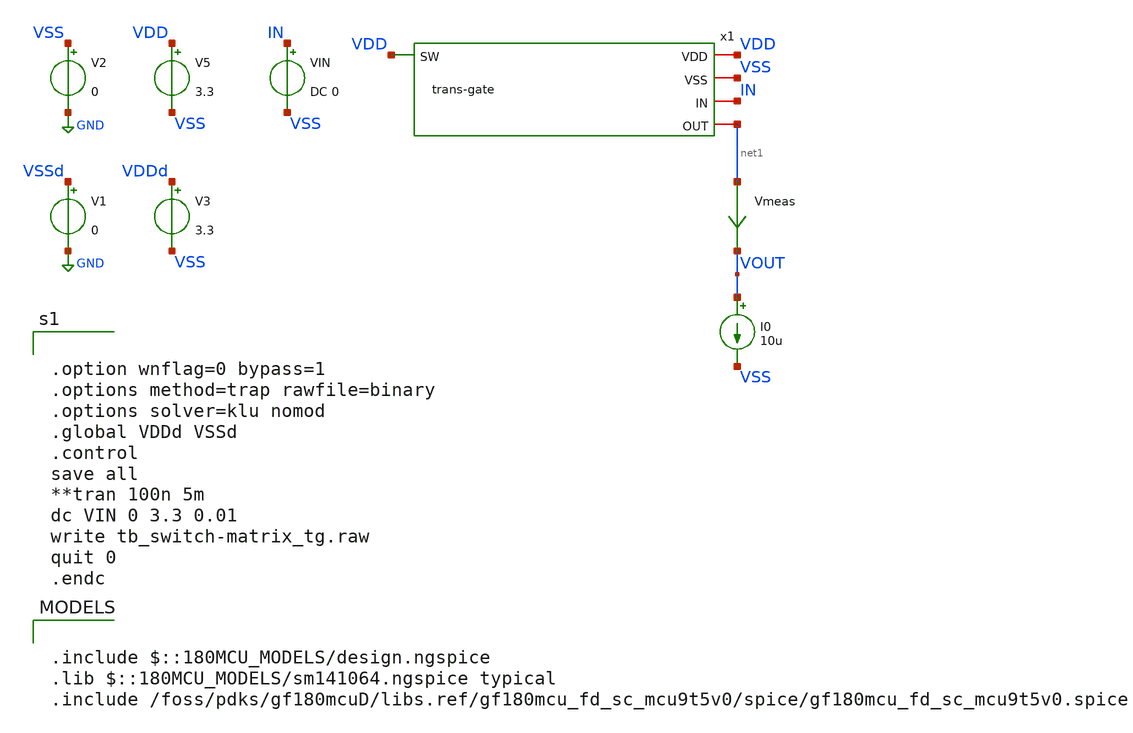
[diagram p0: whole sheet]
** sch_path: designs/libs/core_switch-matrix/tb_switch-matrix/tb_switch-matrix_tg.sch
**.subckt tb_switch-matrix_tg
V2 VSS GND 0
V5 VDD VSS 3.3
VIN IN VSS DC 0
Vmeas net1 VOUT 0
.save i(vmeas)
x1 VDD VSS VDD IN net1 trans-gate
I0 VOUT VSS 10u
V1 VSSd GND 0
V3 VDDd VSS 3.3
**** begin user architecture code


.option wnflag=0 bypass=1
.options method=trap rawfile=binary
.options solver=klu nomod
.global VDDd VSSd
.control
save all
**tran 100n 5m
dc VIN 0 3.3 0.01
write tb_switch-matrix_tg.raw
quit 0
.endc



.include $::180MCU_MODELS/design.ngspice
.lib $::180MCU_MODELS/sm141064.ngspice typical
.include /foss/pdks/gf180mcuD/libs.ref/gf180mcu_fd_sc_mcu9t5v0/spice/gf180mcu_fd_sc_mcu9t5v0.spice

**** end user architecture code
**.ends
.GLOBAL GND
.end
